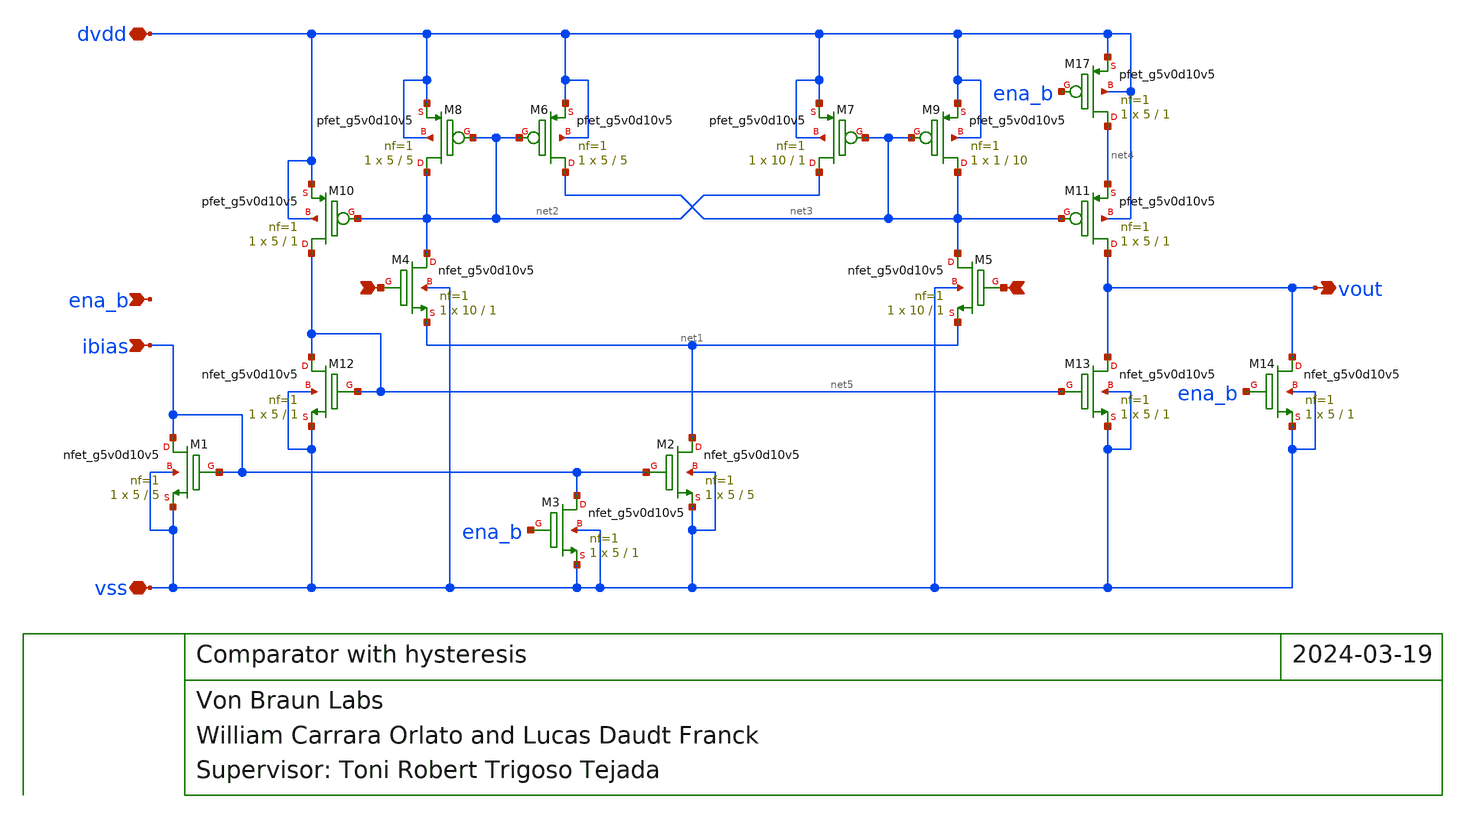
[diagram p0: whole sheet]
** sch_path: xschem_final/comp_hyst.sch
**.subckt comp_hyst vss dvdd ibias - + vout ena_b
*.iopin vss
*.iopin dvdd
*.ipin ibias
*.ipin -
*.ipin +
*.opin vout
*.ipin ena_b
XM17 net4 ena_b dvdd dvdd sky130_fd_pr__pfet_g5v0d10v5 L=1 W=5 nf=1 ad='int((nf+1)/2) * W/nf * 0.29'
+ as='int((nf+2)/2) * W/nf * 0.29' pd='2*int((nf+1)/2) * (W/nf + 0.29)' ps='2*int((nf+2)/2) * (W/nf + 0.29)'
+ nrd='0.29 / W' nrs='0.29 / W' sa=0 sb=0 sd=0 mult=1 m=1
XM1 ibias ibias vss vss sky130_fd_pr__nfet_g5v0d10v5 L=5 W=5 nf=1 ad='int((nf+1)/2) * W/nf * 0.29' as='int((nf+2)/2) * W/nf * 0.29'
+ pd='2*int((nf+1)/2) * (W/nf + 0.29)' ps='2*int((nf+2)/2) * (W/nf + 0.29)' nrd='0.29 / W' nrs='0.29 / W'
+ sa=0 sb=0 sd=0 mult=1 m=1
XM2 net1 ibias vss vss sky130_fd_pr__nfet_g5v0d10v5 L=5 W=5 nf=1 ad='int((nf+1)/2) * W/nf * 0.29' as='int((nf+2)/2) * W/nf * 0.29'
+ pd='2*int((nf+1)/2) * (W/nf + 0.29)' ps='2*int((nf+2)/2) * (W/nf + 0.29)' nrd='0.29 / W' nrs='0.29 / W'
+ sa=0 sb=0 sd=0 mult=1 m=1
XM3 ibias ena_b vss vss sky130_fd_pr__nfet_g5v0d10v5 L=1 W=5 nf=1 ad='int((nf+1)/2) * W/nf * 0.29' as='int((nf+2)/2) * W/nf * 0.29'
+ pd='2*int((nf+1)/2) * (W/nf + 0.29)' ps='2*int((nf+2)/2) * (W/nf + 0.29)' nrd='0.29 / W' nrs='0.29 / W'
+ sa=0 sb=0 sd=0 mult=1 m=1
XM4 net2 - net1 vss sky130_fd_pr__nfet_g5v0d10v5 L=1 W=10 nf=1 ad='int((nf+1)/2) * W/nf * 0.29' as='int((nf+2)/2) * W/nf * 0.29'
+ pd='2*int((nf+1)/2) * (W/nf + 0.29)' ps='2*int((nf+2)/2) * (W/nf + 0.29)' nrd='0.29 / W' nrs='0.29 / W'
+ sa=0 sb=0 sd=0 mult=1 m=1
XM5 net3 + net1 vss sky130_fd_pr__nfet_g5v0d10v5 L=1 W=10 nf=1 ad='int((nf+1)/2) * W/nf * 0.29' as='int((nf+2)/2) * W/nf * 0.29'
+ pd='2*int((nf+1)/2) * (W/nf + 0.29)' ps='2*int((nf+2)/2) * (W/nf + 0.29)' nrd='0.29 / W' nrs='0.29 / W'
+ sa=0 sb=0 sd=0 mult=1 m=1
XM6 net3 net2 dvdd dvdd sky130_fd_pr__pfet_g5v0d10v5 L=5 W=5 nf=1 ad='int((nf+1)/2) * W/nf * 0.29' as='int((nf+2)/2) * W/nf * 0.29'
+ pd='2*int((nf+1)/2) * (W/nf + 0.29)' ps='2*int((nf+2)/2) * (W/nf + 0.29)' nrd='0.29 / W' nrs='0.29 / W'
+ sa=0 sb=0 sd=0 mult=1 m=1
XM7 net2 net3 dvdd dvdd sky130_fd_pr__pfet_g5v0d10v5 L=1 W=10 nf=1 ad='int((nf+1)/2) * W/nf * 0.29' as='int((nf+2)/2) * W/nf * 0.29'
+ pd='2*int((nf+1)/2) * (W/nf + 0.29)' ps='2*int((nf+2)/2) * (W/nf + 0.29)' nrd='0.29 / W' nrs='0.29 / W'
+ sa=0 sb=0 sd=0 mult=1 m=1
XM8 net2 net2 dvdd dvdd sky130_fd_pr__pfet_g5v0d10v5 L=5 W=5 nf=1 ad='int((nf+1)/2) * W/nf * 0.29' as='int((nf+2)/2) * W/nf * 0.29'
+ pd='2*int((nf+1)/2) * (W/nf + 0.29)' ps='2*int((nf+2)/2) * (W/nf + 0.29)' nrd='0.29 / W' nrs='0.29 / W'
+ sa=0 sb=0 sd=0 mult=1 m=1
XM9 net3 net3 dvdd dvdd sky130_fd_pr__pfet_g5v0d10v5 L=10 W=1 nf=1 ad='int((nf+1)/2) * W/nf * 0.29' as='int((nf+2)/2) * W/nf * 0.29'
+ pd='2*int((nf+1)/2) * (W/nf + 0.29)' ps='2*int((nf+2)/2) * (W/nf + 0.29)' nrd='0.29 / W' nrs='0.29 / W'
+ sa=0 sb=0 sd=0 mult=1 m=1
XM10 net5 net2 dvdd dvdd sky130_fd_pr__pfet_g5v0d10v5 L=1 W=5 nf=1 ad='int((nf+1)/2) * W/nf * 0.29' as='int((nf+2)/2) * W/nf * 0.29'
+ pd='2*int((nf+1)/2) * (W/nf + 0.29)' ps='2*int((nf+2)/2) * (W/nf + 0.29)' nrd='0.29 / W' nrs='0.29 / W'
+ sa=0 sb=0 sd=0 mult=1 m=1
XM11 vout net3 net4 dvdd sky130_fd_pr__pfet_g5v0d10v5 L=1 W=5 nf=1 ad='int((nf+1)/2) * W/nf * 0.29' as='int((nf+2)/2) * W/nf * 0.29'
+ pd='2*int((nf+1)/2) * (W/nf + 0.29)' ps='2*int((nf+2)/2) * (W/nf + 0.29)' nrd='0.29 / W' nrs='0.29 / W'
+ sa=0 sb=0 sd=0 mult=1 m=1
XM12 net5 net5 vss vss sky130_fd_pr__nfet_g5v0d10v5 L=1 W=5 nf=1 ad='int((nf+1)/2) * W/nf * 0.29' as='int((nf+2)/2) * W/nf * 0.29'
+ pd='2*int((nf+1)/2) * (W/nf + 0.29)' ps='2*int((nf+2)/2) * (W/nf + 0.29)' nrd='0.29 / W' nrs='0.29 / W'
+ sa=0 sb=0 sd=0 mult=1 m=1
XM13 vout net5 vss vss sky130_fd_pr__nfet_g5v0d10v5 L=1 W=5 nf=1 ad='int((nf+1)/2) * W/nf * 0.29' as='int((nf+2)/2) * W/nf * 0.29'
+ pd='2*int((nf+1)/2) * (W/nf + 0.29)' ps='2*int((nf+2)/2) * (W/nf + 0.29)' nrd='0.29 / W' nrs='0.29 / W'
+ sa=0 sb=0 sd=0 mult=1 m=1
XM14 vout ena_b vss vss sky130_fd_pr__nfet_g5v0d10v5 L=1 W=5 nf=1 ad='int((nf+1)/2) * W/nf * 0.29' as='int((nf+2)/2) * W/nf * 0.29'
+ pd='2*int((nf+1)/2) * (W/nf + 0.29)' ps='2*int((nf+2)/2) * (W/nf + 0.29)' nrd='0.29 / W' nrs='0.29 / W'
+ sa=0 sb=0 sd=0 mult=1 m=1
**.ends
.end
